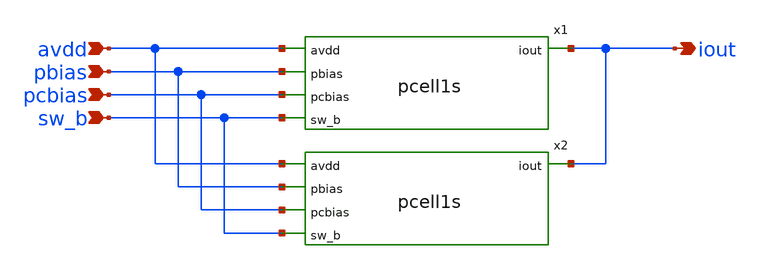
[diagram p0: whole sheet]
** sch_path: xsch/pcell2s.sch
**.subckt pcell2s avdd pbias pcbias sw_b iout
*.ipin avdd
*.ipin pbias
*.ipin pcbias
*.ipin sw_b
*.opin iout
x1 avdd pbias pcbias sw_b iout pcell1s
x2 avdd pbias pcbias sw_b iout pcell1s
**.ends

* expanding   symbol:  idac/pcell1s.sym # of pins=5
** sym_path: idac/pcell1s.sym
** sch_path: idac/pcell1s.sch
.subckt pcell1s avdd pbias pcbias sw_b iout
*.ipin pbias
*.ipin pcbias
*.ipin avdd
*.opin iout
*.ipin sw_b
XM1 net1 pbias avdd avdd sky130_fd_pr__pfet_01v8 L=0.5 W=3 nf=1 ad='int((nf+1)/2) * W/nf * 0.29' as='int((nf+2)/2) * W/nf * 0.29'
+ pd='2*int((nf+1)/2) * (W/nf + 0.29)' ps='2*int((nf+2)/2) * (W/nf + 0.29)' nrd='0.29 / W' nrs='0.29 / W'
+ sa=0 sb=0 sd=0 mult=1 m=1
XM2 net2 pcbias net1 avdd sky130_fd_pr__pfet_01v8 L=0.5 W=6 nf=1 ad='int((nf+1)/2) * W/nf * 0.29' as='int((nf+2)/2) * W/nf * 0.29'
+ pd='2*int((nf+1)/2) * (W/nf + 0.29)' ps='2*int((nf+2)/2) * (W/nf + 0.29)' nrd='0.29 / W' nrs='0.29 / W'
+ sa=0 sb=0 sd=0 mult=1 m=1
XM3 iout sw_b net2 avdd sky130_fd_pr__pfet_01v8 L=0.5 W=2 nf=1 ad='int((nf+1)/2) * W/nf * 0.29' as='int((nf+2)/2) * W/nf * 0.29'
+ pd='2*int((nf+1)/2) * (W/nf + 0.29)' ps='2*int((nf+2)/2) * (W/nf + 0.29)' nrd='0.29 / W' nrs='0.29 / W'
+ sa=0 sb=0 sd=0 mult=1 m=1
.ends

.end
